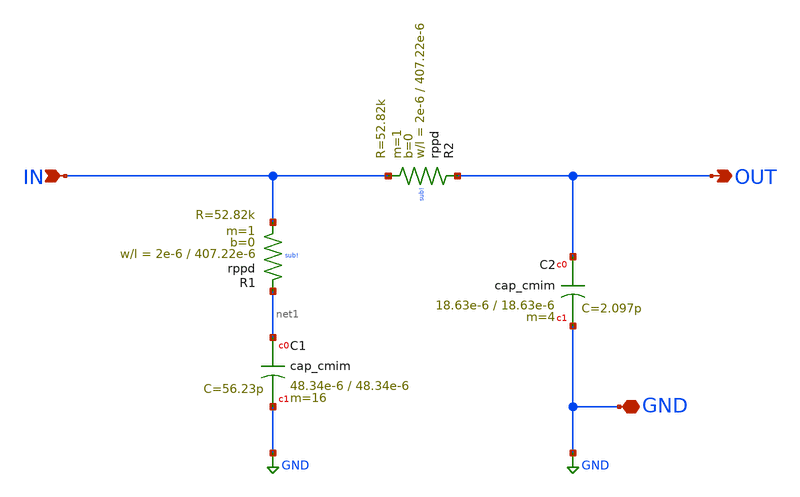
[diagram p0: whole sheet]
** sch_path: schematic/loop-filter/LOOP_FILTER.sch
**.subckt LOOP_FILTER OUT GND IN
*.opin OUT
*.iopin GND
*.ipin IN
XC2 OUT GND cap_cmim w=18.63e-6 l=18.63e-6 m=4 mm_ok=1
XC1 net1 GND cap_cmim w=48.34e-6 l=48.34e-6 m=16 mm_ok=1
XR2 OUT IN sub! rppd w=2e-6 l=407.22e-6 m=1 b=0 mm_ok=1
XR1 net1 IN sub! rppd w=2e-6 l=407.22e-6 m=1 b=0 mm_ok=1
**.ends
.GLOBAL GND
.end
